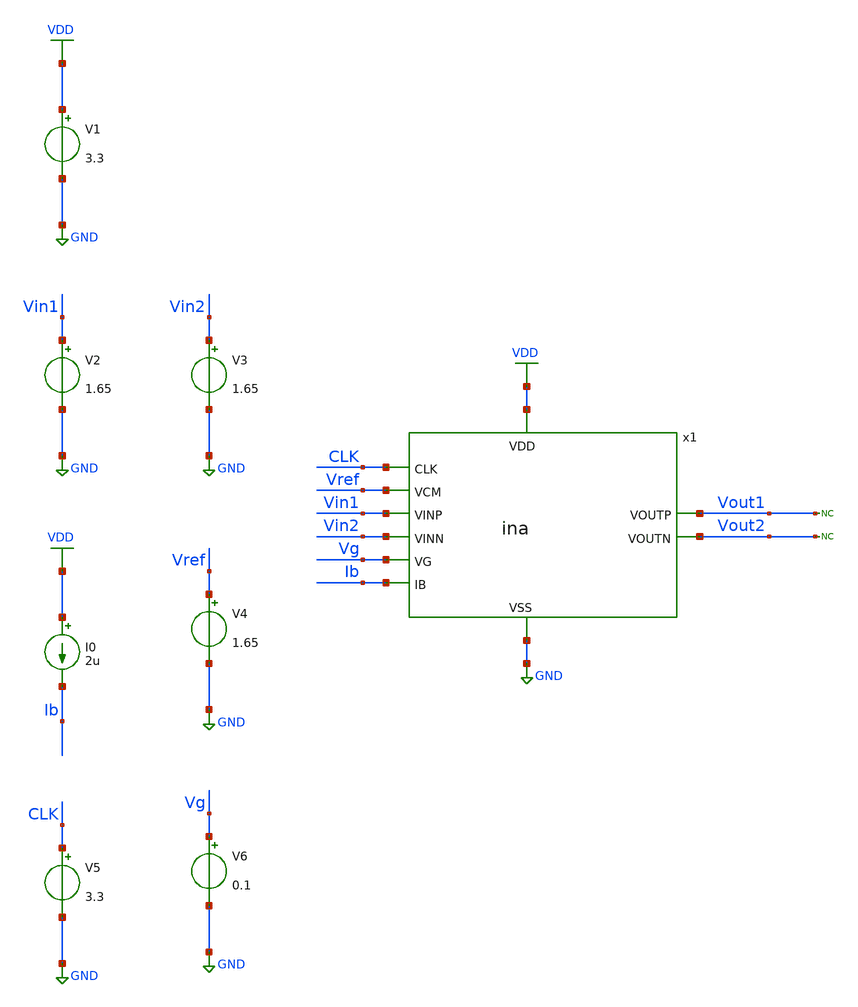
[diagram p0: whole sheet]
** sch_path: designs/libs/tb_ina/tb_ina/tb_ina.sch
**.subckt tb_ina
V1 VDD GND 3.3
V2 Vin1 GND 1.65
V3 Vin2 GND 1.65
I0 VDD Ib 2u
V4 Vref GND 1.65
V5 CLK GND 3.3
V6 Vg GND 0.1
* noconn Vout1
* noconn Vout2
x1 Vg VDD Vin1 Vin2 CLK Vout1 Vout2 GND Vref Ib ina
**** begin user architecture code

.include $::180MCU_MODELS/design.ngspice
.lib $::180MCU_MODELS/sm141064.ngspice typical
.lib $::180MCU_MODELS/sm141064.ngspice cap_mim
.lib $::180MCU_MODELS/sm141064.ngspice moscap_typical
.lib $::180MCU_MODELS/sm141064.ngspice mimcap_typical
.lib $::180MCU_MODELS/sm141064.ngspice res_typical
* .lib $::180MCU_MODELS/sm141064.ngspice res_statistical
* ngspice commands




.control
save all

run
set color0 = white
set appendwrite

*************************************
** PARAMETERS
*************************************

let Vdd  = 3.3
let Vcm  = Vdd/2
let Ibias = 2u
let Vg = 0.1

*************************************
** CHOPPER PARAMETERS
*************************************

let fchop = 4k
let tper = 1/fchop
let ton = tper/2
let tr = 10n
let tf = 10n

*************************************
** SOURCES
*************************************

alter @V2[DC] = $&Vcm
alter @V3[DC] = $&Vcm
alter @V4[DC] = $&Vcm
alter @I0[DC] = $&Ibias
alter @V5[PULSE] = [ 0 $&Vdd 0 $&tr $&tf $&ton $&tper 0 ]
alter @V6[DC] = $&Vg

*************************************
** PVT SIMULATION
*************************************

* AC simulation
alter @V2[ACMAG] = 0.5
alter @V3[ACMAG] = -0.5

* Case 1: VDD = 3.2 V, Temp = -40ºC
alter @V1[DC] = 3.2
set temp = -40
ac dec 100 0.01 100k
let vout_diff = v(Vout1)-v(Vout2)
let vin_diff  = v(Vin1)-v(Vin2)
let Av = vout_diff/vin_diff
let gain_db = db(Av)
meas ac Av0_1 FIND gain_db AT=10

* Case 2: VDD = 3.2 V, Temp = 27ºC
alter @V1[DC] = 3.2
set temp = 27
ac dec 100 0.01 100k
let vout_diff = v(Vout1)-v(Vout2)
let vin_diff  = v(Vin1)-v(Vin2)
let Av = vout_diff/vin_diff
let gain_db = db(Av)
meas ac Av0_2 FIND gain_db AT=10

* Case 3: VDD = 3.2 V, Temp = 125ºC
alter @V1[DC] = 3.2
set temp = 125
ac dec 100 0.01 100k
let vout_diff = v(Vout1)-v(Vout2)
let vin_diff  = v(Vin1)-v(Vin2)
let Av = vout_diff/vin_diff
let gain_db = db(Av)
meas ac Av0_3 FIND gain_db AT=10

* Case 4: VDD = 3.3 V, Temp = -40ºC
alter @V1[DC] = 3.3
set temp = -40
ac dec 100 0.01 100k
let vout_diff = v(Vout1)-v(Vout2)
let vin_diff  = v(Vin1)-v(Vin2)
let Av = vout_diff/vin_diff
let gain_db = db(Av)
meas ac Av0_4 FIND gain_db AT=10

* Case 5: VDD = 3.3 V, Temp = 27ºC
alter @V1[DC] = 3.3
set temp = 27
ac dec 100 0.01 100k
let vout_diff = v(Vout1)-v(Vout2)
let vin_diff  = v(Vin1)-v(Vin2)
let Av = vout_diff/vin_diff
let gain_db = db(Av)
meas ac Av0_5 FIND gain_db AT=10

* Case 6: VDD = 3.3 V, Temp = 125ºC
alter @V1[DC] = 3.3
set temp = 125
ac dec 100 0.01 100k
let vout_diff = v(Vout1)-v(Vout2)
let vin_diff  = v(Vin1)-v(Vin2)
let Av = vout_diff/vin_diff
let gain_db = db(Av)
meas ac Av0_6 FIND gain_db AT=10

* Case 7: VDD = 3.4 V, Temp = -40ºC
alter @V1[DC] = 3.4
set temp = -40
ac dec 100 0.01 100k
let vout_diff = v(Vout1)-v(Vout2)
let vin_diff  = v(Vin1)-v(Vin2)
let Av = vout_diff/vin_diff
let gain_db = db(Av)
meas ac Av0_7 FIND gain_db AT=10

* Case 8: VDD = 3.4 V, Temp = 27ºC
alter @V1[DC] = 3.4
set temp = 27
ac dec 100 0.01 100k
let vout_diff = v(Vout1)-v(Vout2)
let vin_diff  = v(Vin1)-v(Vin2)
let Av = vout_diff/vin_diff
let gain_db = db(Av)
meas ac Av0_8 FIND gain_db AT=10

* Case 9: VDD = 3.4 V, Temp = 125ºC
alter @V1[DC] = 3.4
set temp = 125
ac dec 100 0.01 100k
let vout_diff = v(Vout1)-v(Vout2)
let vin_diff  = v(Vin1)-v(Vin2)
let Av = vout_diff/vin_diff
let gain_db = db(Av)
meas ac Av0_9 FIND gain_db AT=10


* Noise simulation
alter @V2[ACMAG] = 1
alter @V3[ACMAG] = 0
op

* Case 1: VDD = 3.2 V, Temp = -40ºC
alter @V1[DC] = 3.2
set temp = -40
noise v(Vout1) V2 dec 500 0.5 150
setplot noise10
let inoise_rms_1 = inoise_total

* Case 2: VDD = 3.2 V, Temp = 27ºC
alter @V1[DC] = 3.2
set temp = 27
noise v(Vout1) V2 dec 500 0.5 150
setplot noise12
let inoise_rms_2 = inoise_total

* Case 3: VDD = 3.2 V, Temp = 125ºC
alter @V1[DC] = 3.2
set temp = 125
noise v(Vout1) V2 dec 500 0.5 150
setplot noise14
let inoise_rms_3 = inoise_total

* Case 4: VDD = 3.3 V, Temp = -40ºC
alter @V1[DC] = 3.3
set temp = -40
noise v(Vout1) V2 dec 500 0.5 150
setplot noise16
let inoise_rms_4 = inoise_total

* Case 5: VDD = 3.3 V, Temp = 27ºC
alter @V1[DC] = 3.3
set temp = 27
noise v(Vout1) V2 dec 500 0.5 150
setplot noise18
let inoise_rms_5 = inoise_total

* Case 6: VDD = 3.3 V, Temp = 125ºC
alter @V1[DC] = 3.3
set temp = 125
noise v(Vout1) V2 dec 500 0.5 150
setplot noise20
let inoise_rms_6 = inoise_total

* Case 7: VDD = 3.4 V, Temp = -40ºC
alter @V1[DC] = 3.4
set temp = -40
noise v(Vout1) V2 dec 500 0.5 150
setplot noise22
let inoise_rms_7 = inoise_total

* Case 8: VDD = 3.4 V, Temp = 27ºC
alter @V1[DC] = 3.4
set temp = 27
noise v(Vout1) V2 dec 500 0.5 150
setplot noise24
let inoise_rms_8 = inoise_total

* Case 9: VDD = 3.4 V, Temp = 125ºC
alter @V1[DC] = 3.4
set temp = 125
noise v(Vout1) V2 dec 500 0.5 150
setplot noise26
let inoise_rms_9 = inoise_total

*************************************
** PRINTS
*************************************

echo ========================================
echo Case 1: VDD = 3.2 V, Temperature = -40 C
setplot ac1
echo Differential gain : $&Av0_1 dB
setplot noise10
echo Input-Referred Noise : $&inoise_rms_1 Vrms
echo ========================================
echo Case 2: VDD = 3.2 V, Temperature = 27 C
setplot ac2
echo Differential gain : $&Av0_2 dB
setplot noise12
echo Input-Referred Noise : $&inoise_rms_2 Vrms
echo ========================================
echo Case 3: VDD = 3.2 V, Temperature = 125 C
setplot ac3
echo Differential gain : $&Av0_3 dB
setplot noise14
echo Input-Referred Noise : $&inoise_rms_3 µVrms
echo ========================================
echo Case 4: VDD = 3.3 V, Temperature = -40 C
setplot ac4
echo Differential gain : $&Av0_4 dB
setplot noise16
echo Input-Referred Noise : $&inoise_rms_4 Vrms
echo ========================================
echo Case 5: VDD = 3.3 V, Temperature = 27 C
setplot ac5
echo Differential gain : $&Av0_5 dB
setplot noise18
echo Input-Referred Noise : $&inoise_rms_5 Vrms
echo ========================================
echo Case 6: VDD = 3.3 V, Temperature = 125 C
setplot ac6
echo Differential gain : $&Av0_6 dB
setplot noise20
echo Input-Referred Noise : $&inoise_rms_6 Vrms
echo ========================================
echo Case 7: VDD = 3.4 V, Temperature = -40 C
setplot ac7
echo Differential gain : $&Av0_7 dB
setplot noise22
echo Input-Referred Noise : $&inoise_rms_7 Vrms
echo ========================================
echo Case 8: VDD = 3.4 V, Temperature = 27 C
setplot ac8
echo Differential gain : $&Av0_8 dB
setplot noise24
echo Input-Referred Noise : $&inoise_rms_8 Vrms
echo ========================================
echo Case 9: VDD = 3.4 V, Temperature = 125 C
setplot ac9
echo Differential gain : $&Av0_9 dB
setplot noise26
echo Input-Referred Noise : $&inoise_rms_9 Vrms
echo ========================================

*************************************
** SAVE
*************************************

write tb_ina.raw

.endc
* ngspice commands



**** end user architecture code
**.ends
.GLOBAL GND
.GLOBAL VDD
.end
